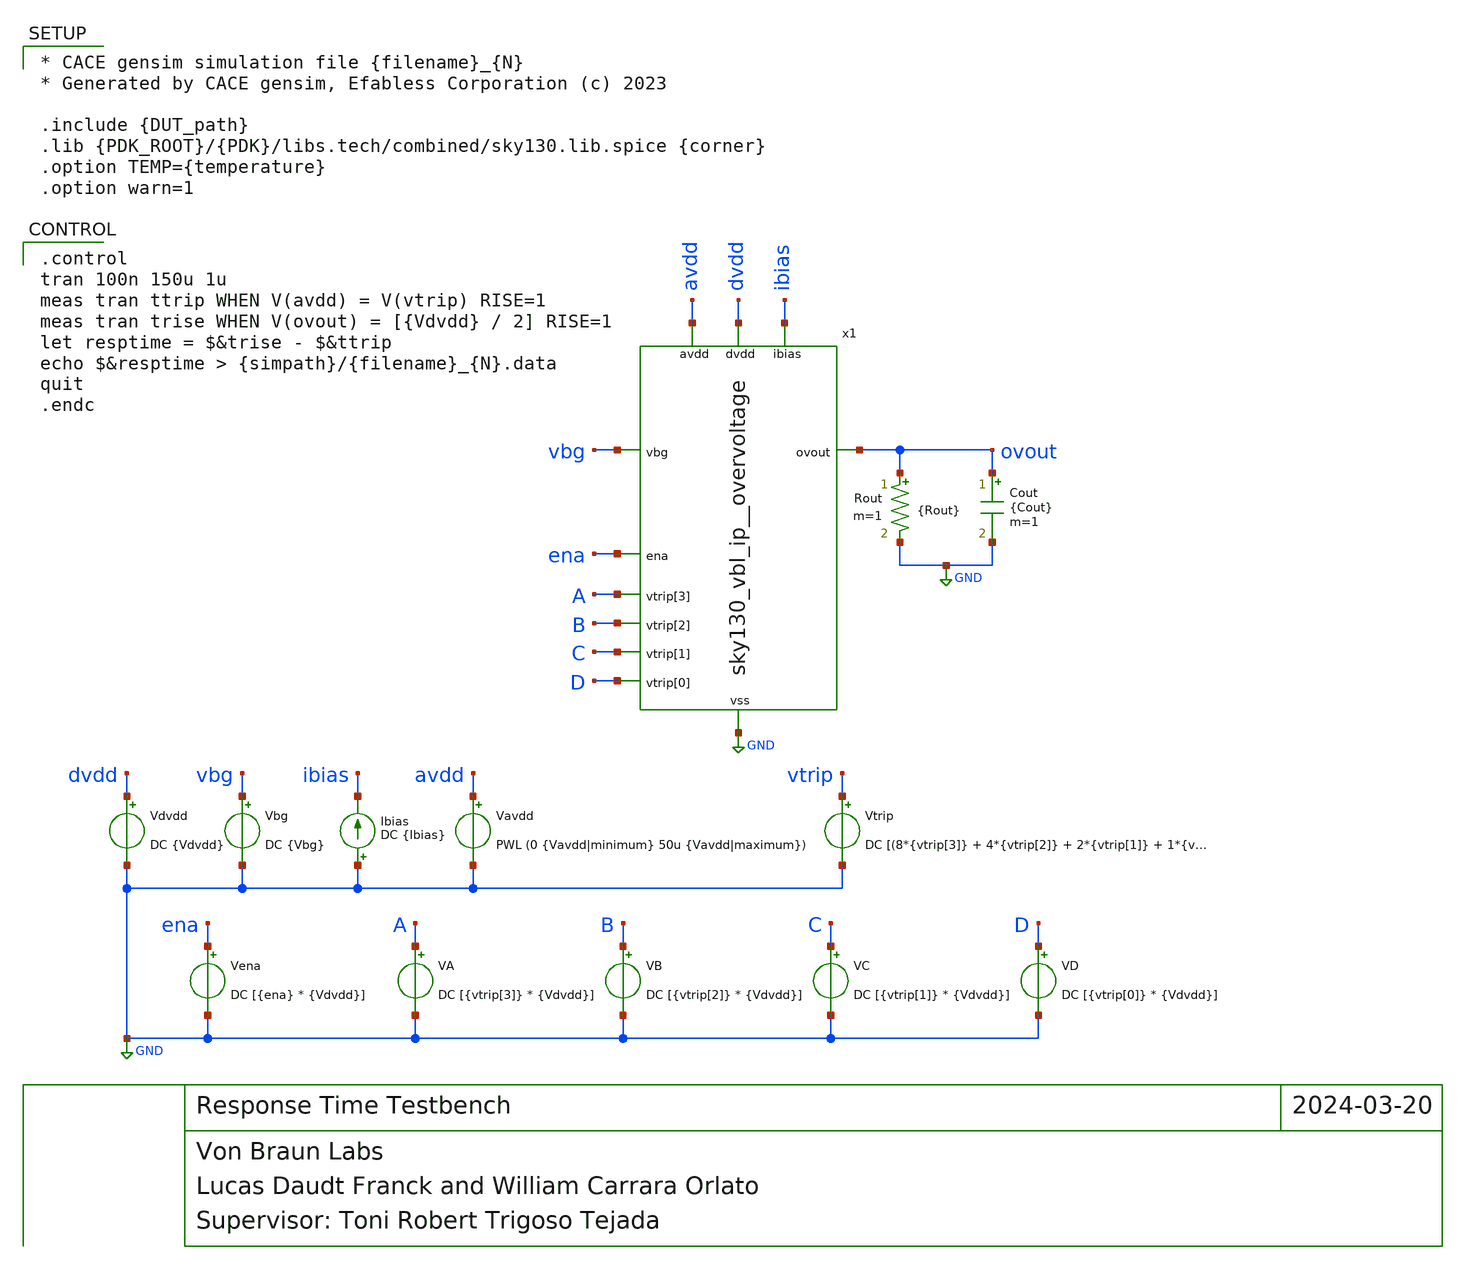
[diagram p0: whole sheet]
** sch_path: cace/tb_resptime.sch
**.subckt tb_resptime
Vavdd avdd GND PWL (0 {Vavdd|minimum} 50u {Vavdd|maximum})
Vdvdd dvdd GND DC {Vdvdd}
Vbg vbg GND DC {Vbg}
Ibias GND ibias DC {Ibias}
Vtrip vtrip GND DC [(8*{vtrip[3]} + 4*{vtrip[2]} + 2*{vtrip[1]} + 1*{vtrip[0]})*0.14667 + 3.3]
Vena ena GND DC [{ena} * {Vdvdd}]
VA A GND DC [{vtrip[3]} * {Vdvdd}]
VB B GND DC [{vtrip[2]} * {Vdvdd}]
VC C GND DC [{vtrip[1]} * {Vdvdd}]
VD D GND DC [{vtrip[0]} * {Vdvdd}]
Cout ovout GND {Cout} m=1
Rout ovout GND {Rout} m=1
x1 avdd dvdd ena A GND ibias B ovout vbg C D sky130_vbl_ip__overvoltage
**** begin user architecture code

* CACE gensim simulation file {filename}_{N}
* Generated by CACE gensim, Efabless Corporation (c) 2023

.include {DUT_path}
.lib {PDK_ROOT}/{PDK}/libs.tech/combined/sky130.lib.spice {corner}
.option TEMP={temperature}
.option warn=1



.control
tran 100n 150u 1u
meas tran ttrip WHEN V(avdd) = V(vtrip) RISE=1
meas tran trise WHEN V(ovout) = [{Vdvdd} / 2] RISE=1
let resptime = $&trise - $&ttrip
echo $&resptime > {simpath}/{filename}_{N}.data
quit
.endc


**** end user architecture code
**.ends
.GLOBAL GND
.end
